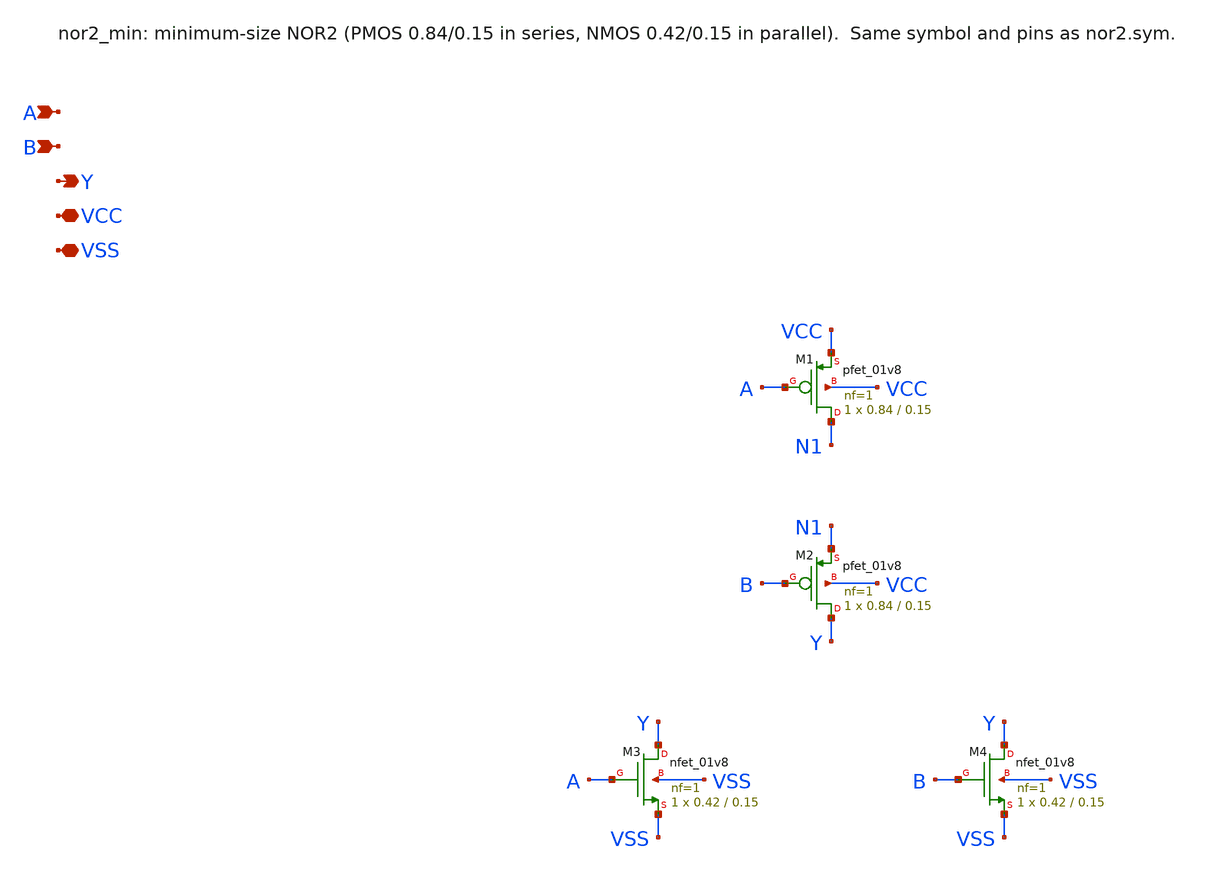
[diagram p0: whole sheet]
** sch_path: SAR_improved/nor2_min.sch
**.subckt nor2_min A B Y VCC VSS
*.ipin A
*.ipin B
*.opin Y
*.iopin VCC
*.iopin VSS
XM1 N1 A VCC VCC sky130_fd_pr__pfet_01v8 L=0.15 W=0.84 nf=1 ad='int((nf+1)/2) * W/nf * 0.29' as='int((nf+2)/2) * W/nf * 0.29'
+ pd='2*int((nf+1)/2) * (W/nf + 0.29)' ps='2*int((nf+2)/2) * (W/nf + 0.29)' nrd='0.29 / W' nrs='0.29 / W'
+ sa=0 sb=0 sd=0 mult=1 m=1
XM2 Y B N1 VCC sky130_fd_pr__pfet_01v8 L=0.15 W=0.84 nf=1 ad='int((nf+1)/2) * W/nf * 0.29' as='int((nf+2)/2) * W/nf * 0.29'
+ pd='2*int((nf+1)/2) * (W/nf + 0.29)' ps='2*int((nf+2)/2) * (W/nf + 0.29)' nrd='0.29 / W' nrs='0.29 / W'
+ sa=0 sb=0 sd=0 mult=1 m=1
XM3 Y A VSS VSS sky130_fd_pr__nfet_01v8 L=0.15 W=0.42 nf=1 ad='int((nf+1)/2) * W/nf * 0.29' as='int((nf+2)/2) * W/nf * 0.29'
+ pd='2*int((nf+1)/2) * (W/nf + 0.29)' ps='2*int((nf+2)/2) * (W/nf + 0.29)' nrd='0.29 / W' nrs='0.29 / W'
+ sa=0 sb=0 sd=0 mult=1 m=1
XM4 Y B VSS VSS sky130_fd_pr__nfet_01v8 L=0.15 W=0.42 nf=1 ad='int((nf+1)/2) * W/nf * 0.29' as='int((nf+2)/2) * W/nf * 0.29'
+ pd='2*int((nf+1)/2) * (W/nf + 0.29)' ps='2*int((nf+2)/2) * (W/nf + 0.29)' nrd='0.29 / W' nrs='0.29 / W'
+ sa=0 sb=0 sd=0 mult=1 m=1
**.ends
.end
